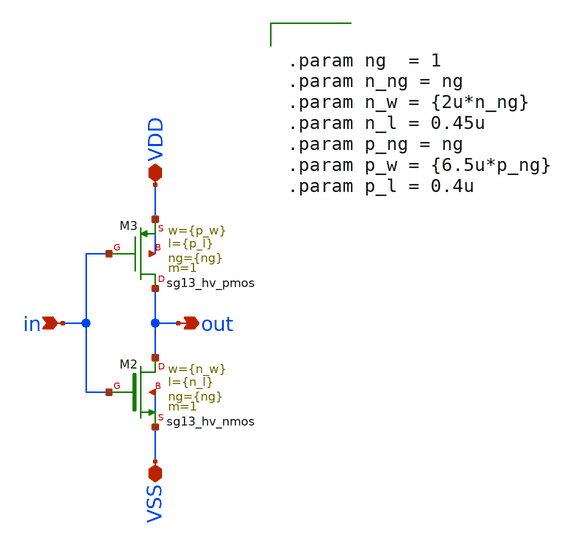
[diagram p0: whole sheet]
** sch_path: macros/heichips26_vcr/macros/switched_capacitor/schematic/xschem/hv_inverter_6u5.sch
**.subckt hv_inverter_6u5 in VDD VSS out
*.ipin in
*.iopin VDD
*.iopin VSS
*.opin out
XM2 out in VSS VSS sg13_hv_nmos w={n_w} l={n_l} ng={ng} m=1 mm_ok=1
XM3 out in VDD VDD sg13_hv_pmos w={p_w} l={p_l} ng={ng} m=1 mm_ok=1
**** begin user architecture code


.param ng  = 1
.param n_ng = ng
.param n_w = {2u*n_ng}
.param n_l = 0.45u
.param p_ng = ng
.param p_w = {6.5u*p_ng}
.param p_l = 0.4u


**** end user architecture code
**.ends
.end
